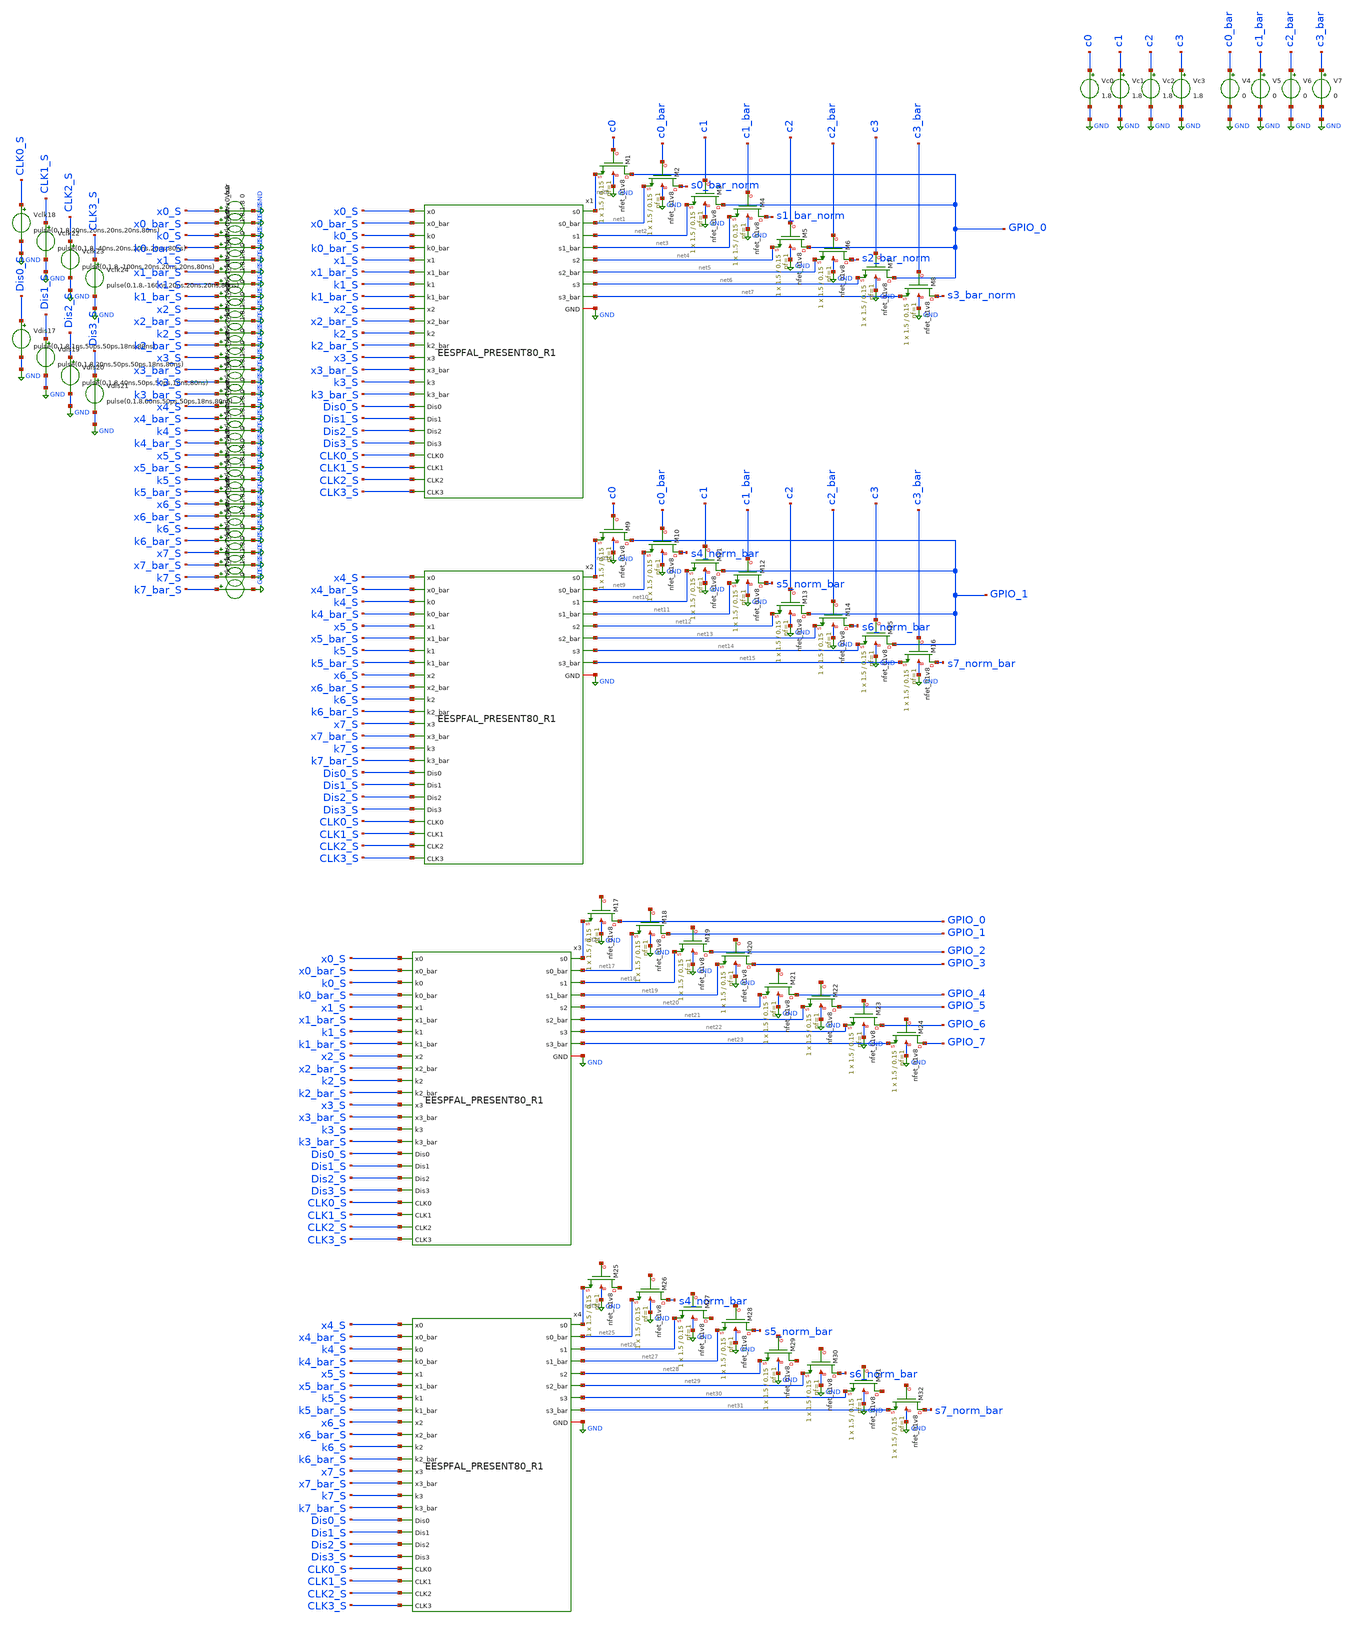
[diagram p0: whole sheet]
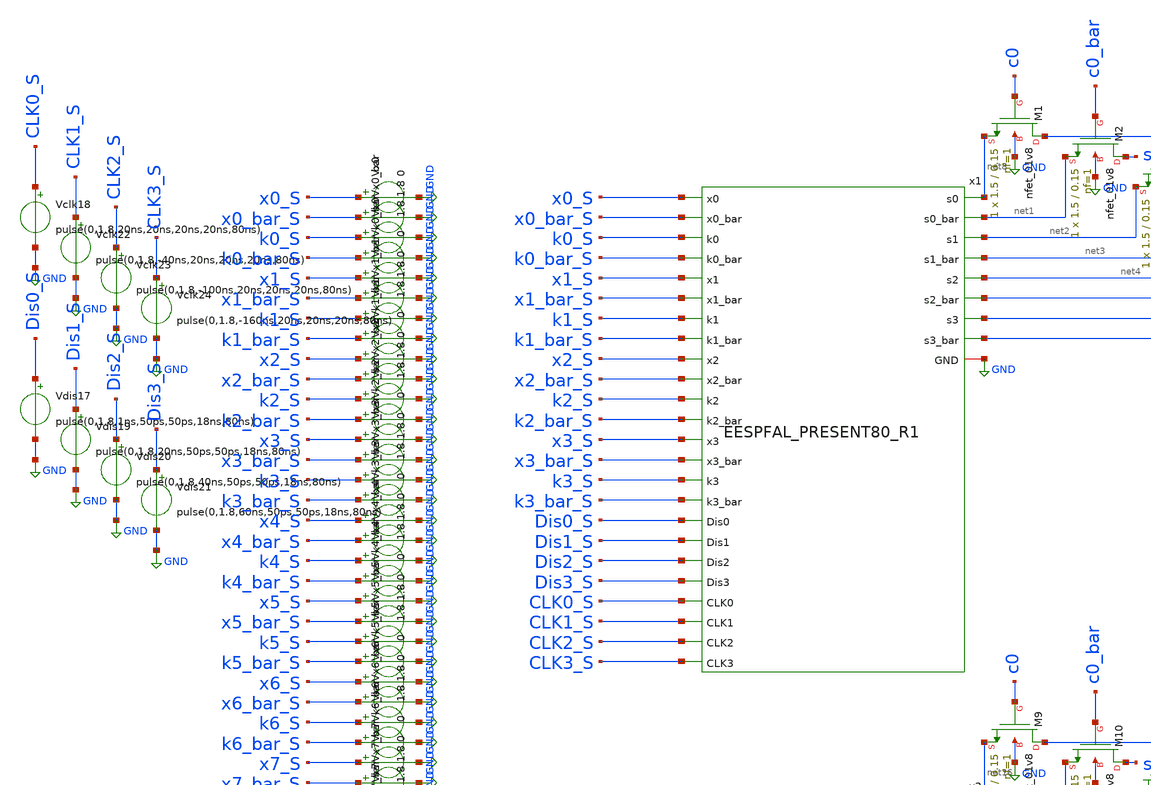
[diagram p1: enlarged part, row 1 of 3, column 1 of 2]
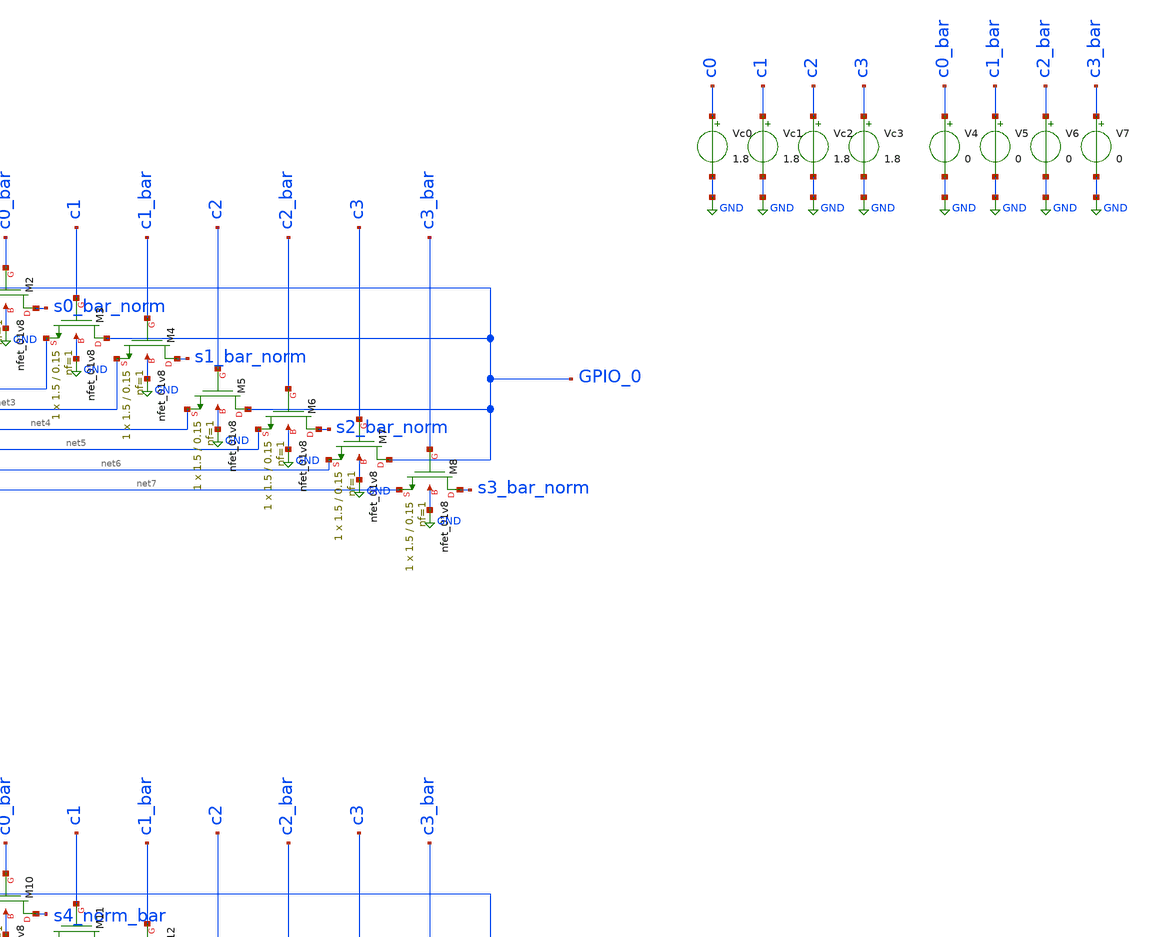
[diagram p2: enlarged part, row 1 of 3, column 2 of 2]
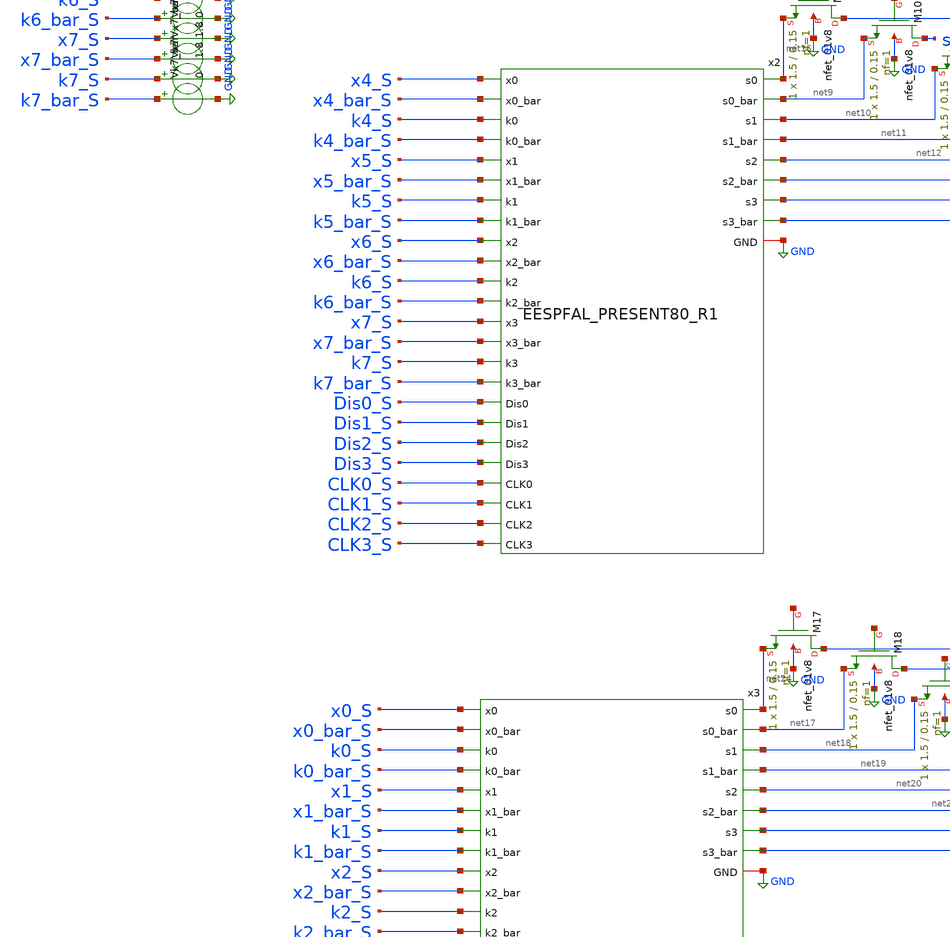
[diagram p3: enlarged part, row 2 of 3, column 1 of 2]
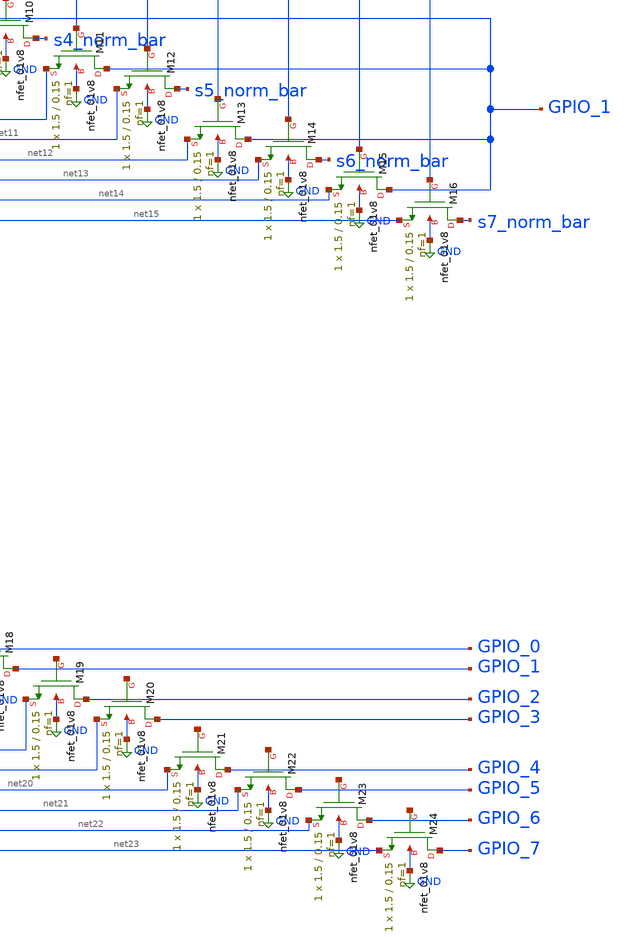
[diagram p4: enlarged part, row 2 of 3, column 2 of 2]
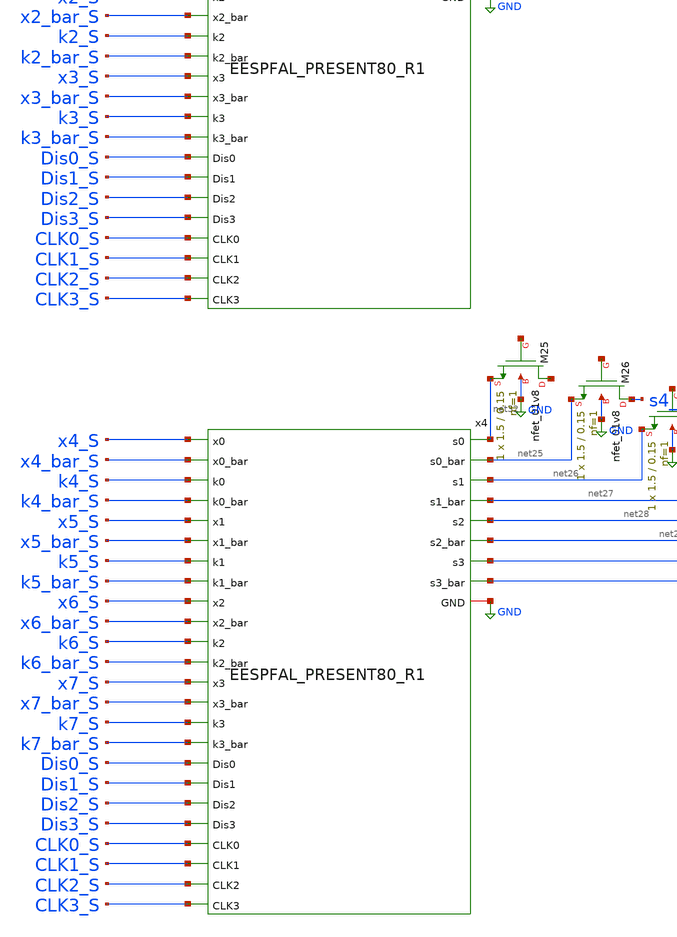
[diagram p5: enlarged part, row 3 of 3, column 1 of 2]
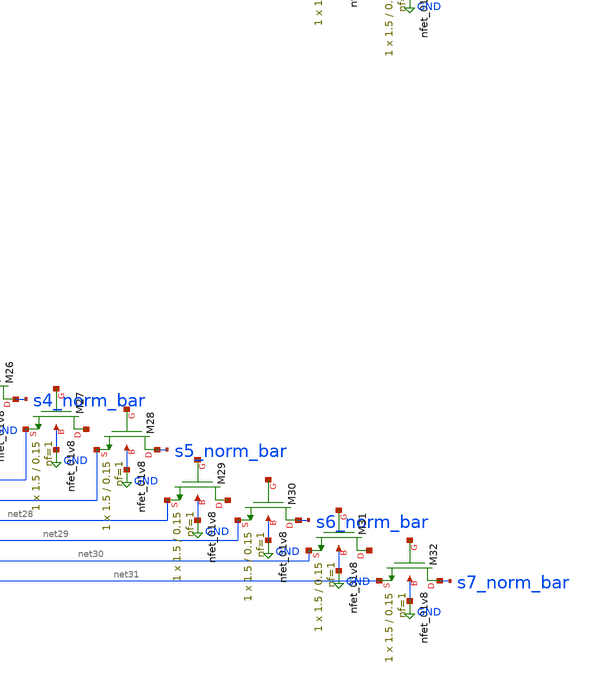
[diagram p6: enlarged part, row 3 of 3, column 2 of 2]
** sch_path: skywater_stuff/EESPFAL_PRESENT80_R1_select_output.sch
**.subckt EESPFAL_PRESENT80_R1_select_output
Vdis17 Dis0_S GND pulse(0,1.8,1ns,50ps,50ps,18ns,80ns)
Vclk18 CLK0_S GND pulse(0,1.8,20ns,20ns,20ns,20ns,80ns)
Vdis19 Dis1_S GND pulse(0,1.8,20ns,50ps,50ps,18ns,80ns)
Vdis20 Dis2_S GND pulse(0,1.8,40ns,50ps,50ps,18ns,80ns)
Vdis21 Dis3_S GND pulse(0,1.8,60ns,50ps,50ps,18ns,80ns)
Vclk22 CLK1_S GND pulse(0,1.8,-40ns,20ns,20ns,20ns,80ns)
Vclk23 CLK2_S GND pulse(0,1.8,-100ns,20ns,20ns,20ns,80ns)
Vclk24 CLK3_S GND pulse(0,1.8,-160ns,20ns,20ns,20ns,80ns)
Vx0 x0_S GND 0
Vx0_bar x0_bar_S GND 1.8
Vk0 k0_S GND 1.8
Vk0_bar k0_bar_S GND 0
Vx1 x1_S GND 0
Vx1_bar x1_bar_S GND 1.8
Vk1 k1_S GND 1.8
Vk1_bar k1_bar_S GND 0
Vx2 x2_S GND 0
Vx2_bar x2_bar_S GND 1.8
Vk2 k2_S GND 1.8
Vk2_bar k2_bar_S GND 0
Vx3 x3_S GND 0
Vx3_bar x3_bar_S GND 1.8
Vk3 k3_S GND 1.8
Vk3_bar k3_bar_S GND 0
Vx4 x4_S GND 0
Vx4_bar x4_bar_S GND 1.8
Vk4 k4_S GND 1.8
Vk4_bar k4_bar_S GND 0
Vx5 x5_S GND 0
Vx5_bar x5_bar_S GND 1.8
Vk5 k5_S GND 1.8
Vk5_bar k5_bar_S GND 0
Vx6 x6_S GND 0
Vx6_bar x6_bar_S GND 1.8
Vk6 k6_S GND 1.8
Vk6_bar k6_bar_S GND 0
Vx7 x7_S GND 0
Vx7_bar x7_bar_S GND 1.8
Vk7 k7_S GND 1.8
Vk7_bar k7_bar_S GND 0
x1 GND x0_S x0_bar_S k0_S k0_bar_S x1_S x1_bar_S k1_S k1_bar_S x2_S x2_bar_S k2_S k2_bar_S x3_S
+ x3_bar_S k3_S k3_bar_S net8 net1 CLK0_S Dis0_S CLK1_S Dis1_S net4 net5 net7 net6 net3 net2 CLK3_S Dis2_S
+ CLK2_S Dis3_S EESPFAL_PRESENT80_R1
x2 GND x4_S x4_bar_S k4_S k4_bar_S x5_S x5_bar_S k5_S k5_bar_S x6_S x6_bar_S k6_S k6_bar_S x7_S
+ x7_bar_S k7_S k7_bar_S net16 net9 CLK0_S Dis0_S CLK1_S Dis1_S net12 net13 net15 net14 net11 net10 CLK3_S
+ Dis2_S CLK2_S Dis3_S EESPFAL_PRESENT80_R1
XM1 GPIO_0 c0 net8 GND sky130_fd_pr__nfet_01v8 L=0.15 W=1.5 nf=1 ad='int((nf+1)/2) * W/nf * 0.29' as='int((nf+2)/2) * W/nf * 0.29'
+ pd='2*int((nf+1)/2) * (W/nf + 0.29)' ps='2*int((nf+2)/2) * (W/nf + 0.29)' nrd='0.29 / W' nrs='0.29 / W'
+ sa=0 sb=0 sd=0 mult=1 m=1
XM2 s0_bar_norm c0_bar net1 GND sky130_fd_pr__nfet_01v8 L=0.15 W=1.5 nf=1 ad='int((nf+1)/2) * W/nf * 0.29'
+ as='int((nf+2)/2) * W/nf * 0.29' pd='2*int((nf+1)/2) * (W/nf + 0.29)' ps='2*int((nf+2)/2) * (W/nf + 0.29)'
+ nrd='0.29 / W' nrs='0.29 / W' sa=0 sb=0 sd=0 mult=1 m=1
XM3 GPIO_0 c1 net2 GND sky130_fd_pr__nfet_01v8 L=0.15 W=1.5 nf=1 ad='int((nf+1)/2) * W/nf * 0.29' as='int((nf+2)/2) * W/nf * 0.29'
+ pd='2*int((nf+1)/2) * (W/nf + 0.29)' ps='2*int((nf+2)/2) * (W/nf + 0.29)' nrd='0.29 / W' nrs='0.29 / W'
+ sa=0 sb=0 sd=0 mult=1 m=1
XM4 s1_bar_norm c1_bar net3 GND sky130_fd_pr__nfet_01v8 L=0.15 W=1.5 nf=1 ad='int((nf+1)/2) * W/nf * 0.29'
+ as='int((nf+2)/2) * W/nf * 0.29' pd='2*int((nf+1)/2) * (W/nf + 0.29)' ps='2*int((nf+2)/2) * (W/nf + 0.29)'
+ nrd='0.29 / W' nrs='0.29 / W' sa=0 sb=0 sd=0 mult=1 m=1
XM5 GPIO_0 c2 net4 GND sky130_fd_pr__nfet_01v8 L=0.15 W=1.5 nf=1 ad='int((nf+1)/2) * W/nf * 0.29' as='int((nf+2)/2) * W/nf * 0.29'
+ pd='2*int((nf+1)/2) * (W/nf + 0.29)' ps='2*int((nf+2)/2) * (W/nf + 0.29)' nrd='0.29 / W' nrs='0.29 / W'
+ sa=0 sb=0 sd=0 mult=1 m=1
XM6 s2_bar_norm c2_bar net5 GND sky130_fd_pr__nfet_01v8 L=0.15 W=1.5 nf=1 ad='int((nf+1)/2) * W/nf * 0.29'
+ as='int((nf+2)/2) * W/nf * 0.29' pd='2*int((nf+1)/2) * (W/nf + 0.29)' ps='2*int((nf+2)/2) * (W/nf + 0.29)'
+ nrd='0.29 / W' nrs='0.29 / W' sa=0 sb=0 sd=0 mult=1 m=1
XM7 GPIO_0 c3 net6 GND sky130_fd_pr__nfet_01v8 L=0.15 W=1.5 nf=1 ad='int((nf+1)/2) * W/nf * 0.29' as='int((nf+2)/2) * W/nf * 0.29'
+ pd='2*int((nf+1)/2) * (W/nf + 0.29)' ps='2*int((nf+2)/2) * (W/nf + 0.29)' nrd='0.29 / W' nrs='0.29 / W'
+ sa=0 sb=0 sd=0 mult=1 m=1
XM8 s3_bar_norm c3_bar net7 GND sky130_fd_pr__nfet_01v8 L=0.15 W=1.5 nf=1 ad='int((nf+1)/2) * W/nf * 0.29'
+ as='int((nf+2)/2) * W/nf * 0.29' pd='2*int((nf+1)/2) * (W/nf + 0.29)' ps='2*int((nf+2)/2) * (W/nf + 0.29)'
+ nrd='0.29 / W' nrs='0.29 / W' sa=0 sb=0 sd=0 mult=1 m=1
XM9 GPIO_1 c0 net16 GND sky130_fd_pr__nfet_01v8 L=0.15 W=1.5 nf=1 ad='int((nf+1)/2) * W/nf * 0.29' as='int((nf+2)/2) * W/nf * 0.29'
+ pd='2*int((nf+1)/2) * (W/nf + 0.29)' ps='2*int((nf+2)/2) * (W/nf + 0.29)' nrd='0.29 / W' nrs='0.29 / W'
+ sa=0 sb=0 sd=0 mult=1 m=1
XM10 s4_norm_bar c0_bar net9 GND sky130_fd_pr__nfet_01v8 L=0.15 W=1.5 nf=1 ad='int((nf+1)/2) * W/nf * 0.29'
+ as='int((nf+2)/2) * W/nf * 0.29' pd='2*int((nf+1)/2) * (W/nf + 0.29)' ps='2*int((nf+2)/2) * (W/nf + 0.29)'
+ nrd='0.29 / W' nrs='0.29 / W' sa=0 sb=0 sd=0 mult=1 m=1
XM11 GPIO_1 c1 net10 GND sky130_fd_pr__nfet_01v8 L=0.15 W=1.5 nf=1 ad='int((nf+1)/2) * W/nf * 0.29' as='int((nf+2)/2) * W/nf * 0.29'
+ pd='2*int((nf+1)/2) * (W/nf + 0.29)' ps='2*int((nf+2)/2) * (W/nf + 0.29)' nrd='0.29 / W' nrs='0.29 / W'
+ sa=0 sb=0 sd=0 mult=1 m=1
XM12 s5_norm_bar c1_bar net11 GND sky130_fd_pr__nfet_01v8 L=0.15 W=1.5 nf=1 ad='int((nf+1)/2) * W/nf * 0.29'
+ as='int((nf+2)/2) * W/nf * 0.29' pd='2*int((nf+1)/2) * (W/nf + 0.29)' ps='2*int((nf+2)/2) * (W/nf + 0.29)'
+ nrd='0.29 / W' nrs='0.29 / W' sa=0 sb=0 sd=0 mult=1 m=1
XM13 GPIO_1 c2 net12 GND sky130_fd_pr__nfet_01v8 L=0.15 W=1.5 nf=1 ad='int((nf+1)/2) * W/nf * 0.29' as='int((nf+2)/2) * W/nf * 0.29'
+ pd='2*int((nf+1)/2) * (W/nf + 0.29)' ps='2*int((nf+2)/2) * (W/nf + 0.29)' nrd='0.29 / W' nrs='0.29 / W'
+ sa=0 sb=0 sd=0 mult=1 m=1
XM14 s6_norm_bar c2_bar net13 GND sky130_fd_pr__nfet_01v8 L=0.15 W=1.5 nf=1 ad='int((nf+1)/2) * W/nf * 0.29'
+ as='int((nf+2)/2) * W/nf * 0.29' pd='2*int((nf+1)/2) * (W/nf + 0.29)' ps='2*int((nf+2)/2) * (W/nf + 0.29)'
+ nrd='0.29 / W' nrs='0.29 / W' sa=0 sb=0 sd=0 mult=1 m=1
XM15 GPIO_1 c3 net14 GND sky130_fd_pr__nfet_01v8 L=0.15 W=1.5 nf=1 ad='int((nf+1)/2) * W/nf * 0.29' as='int((nf+2)/2) * W/nf * 0.29'
+ pd='2*int((nf+1)/2) * (W/nf + 0.29)' ps='2*int((nf+2)/2) * (W/nf + 0.29)' nrd='0.29 / W' nrs='0.29 / W'
+ sa=0 sb=0 sd=0 mult=1 m=1
XM16 s7_norm_bar c3_bar net15 GND sky130_fd_pr__nfet_01v8 L=0.15 W=1.5 nf=1 ad='int((nf+1)/2) * W/nf * 0.29'
+ as='int((nf+2)/2) * W/nf * 0.29' pd='2*int((nf+1)/2) * (W/nf + 0.29)' ps='2*int((nf+2)/2) * (W/nf + 0.29)'
+ nrd='0.29 / W' nrs='0.29 / W' sa=0 sb=0 sd=0 mult=1 m=1
Vc0 c0 GND 1.8
Vc1 c1 GND 1.8
Vc2 c2 GND 1.8
Vc3 c3 GND 1.8
V4 c0_bar GND 0
V5 c1_bar GND 0
V6 c2_bar GND 0
V7 c3_bar GND 0
x3 GND x0_S x0_bar_S k0_S k0_bar_S x1_S x1_bar_S k1_S k1_bar_S x2_S x2_bar_S k2_S k2_bar_S x3_S
+ x3_bar_S k3_S k3_bar_S net24 net17 CLK0_S Dis0_S CLK1_S Dis1_S net20 net21 net23 net22 net19 net18 CLK3_S
+ Dis2_S CLK2_S Dis3_S EESPFAL_PRESENT80_R1
x4 GND x4_S x4_bar_S k4_S k4_bar_S x5_S x5_bar_S k5_S k5_bar_S x6_S x6_bar_S k6_S k6_bar_S x7_S
+ x7_bar_S k7_S k7_bar_S net32 net25 CLK0_S Dis0_S CLK1_S Dis1_S net28 net29 net31 net30 net27 net26 CLK3_S
+ Dis2_S CLK2_S Dis3_S EESPFAL_PRESENT80_R1
XM17 GPIO_0 net33 net24 GND sky130_fd_pr__nfet_01v8 L=0.15 W=1.5 nf=1 ad='int((nf+1)/2) * W/nf * 0.29'
+ as='int((nf+2)/2) * W/nf * 0.29' pd='2*int((nf+1)/2) * (W/nf + 0.29)' ps='2*int((nf+2)/2) * (W/nf + 0.29)'
+ nrd='0.29 / W' nrs='0.29 / W' sa=0 sb=0 sd=0 mult=1 m=1
XM18 GPIO_1 net34 net17 GND sky130_fd_pr__nfet_01v8 L=0.15 W=1.5 nf=1 ad='int((nf+1)/2) * W/nf * 0.29'
+ as='int((nf+2)/2) * W/nf * 0.29' pd='2*int((nf+1)/2) * (W/nf + 0.29)' ps='2*int((nf+2)/2) * (W/nf + 0.29)'
+ nrd='0.29 / W' nrs='0.29 / W' sa=0 sb=0 sd=0 mult=1 m=1
XM19 GPIO_2 net35 net18 GND sky130_fd_pr__nfet_01v8 L=0.15 W=1.5 nf=1 ad='int((nf+1)/2) * W/nf * 0.29'
+ as='int((nf+2)/2) * W/nf * 0.29' pd='2*int((nf+1)/2) * (W/nf + 0.29)' ps='2*int((nf+2)/2) * (W/nf + 0.29)'
+ nrd='0.29 / W' nrs='0.29 / W' sa=0 sb=0 sd=0 mult=1 m=1
XM20 GPIO_3 net36 net19 GND sky130_fd_pr__nfet_01v8 L=0.15 W=1.5 nf=1 ad='int((nf+1)/2) * W/nf * 0.29'
+ as='int((nf+2)/2) * W/nf * 0.29' pd='2*int((nf+1)/2) * (W/nf + 0.29)' ps='2*int((nf+2)/2) * (W/nf + 0.29)'
+ nrd='0.29 / W' nrs='0.29 / W' sa=0 sb=0 sd=0 mult=1 m=1
XM21 GPIO_4 net37 net20 GND sky130_fd_pr__nfet_01v8 L=0.15 W=1.5 nf=1 ad='int((nf+1)/2) * W/nf * 0.29'
+ as='int((nf+2)/2) * W/nf * 0.29' pd='2*int((nf+1)/2) * (W/nf + 0.29)' ps='2*int((nf+2)/2) * (W/nf + 0.29)'
+ nrd='0.29 / W' nrs='0.29 / W' sa=0 sb=0 sd=0 mult=1 m=1
XM22 GPIO_5 net38 net21 GND sky130_fd_pr__nfet_01v8 L=0.15 W=1.5 nf=1 ad='int((nf+1)/2) * W/nf * 0.29'
+ as='int((nf+2)/2) * W/nf * 0.29' pd='2*int((nf+1)/2) * (W/nf + 0.29)' ps='2*int((nf+2)/2) * (W/nf + 0.29)'
+ nrd='0.29 / W' nrs='0.29 / W' sa=0 sb=0 sd=0 mult=1 m=1
XM23 GPIO_6 net39 net22 GND sky130_fd_pr__nfet_01v8 L=0.15 W=1.5 nf=1 ad='int((nf+1)/2) * W/nf * 0.29'
+ as='int((nf+2)/2) * W/nf * 0.29' pd='2*int((nf+1)/2) * (W/nf + 0.29)' ps='2*int((nf+2)/2) * (W/nf + 0.29)'
+ nrd='0.29 / W' nrs='0.29 / W' sa=0 sb=0 sd=0 mult=1 m=1
XM24 GPIO_7 net40 net23 GND sky130_fd_pr__nfet_01v8 L=0.15 W=1.5 nf=1 ad='int((nf+1)/2) * W/nf * 0.29'
+ as='int((nf+2)/2) * W/nf * 0.29' pd='2*int((nf+1)/2) * (W/nf + 0.29)' ps='2*int((nf+2)/2) * (W/nf + 0.29)'
+ nrd='0.29 / W' nrs='0.29 / W' sa=0 sb=0 sd=0 mult=1 m=1
XM25 net41 net42 net32 GND sky130_fd_pr__nfet_01v8 L=0.15 W=1.5 nf=1 ad='int((nf+1)/2) * W/nf * 0.29'
+ as='int((nf+2)/2) * W/nf * 0.29' pd='2*int((nf+1)/2) * (W/nf + 0.29)' ps='2*int((nf+2)/2) * (W/nf + 0.29)'
+ nrd='0.29 / W' nrs='0.29 / W' sa=0 sb=0 sd=0 mult=1 m=1
XM26 s4_norm_bar net43 net25 GND sky130_fd_pr__nfet_01v8 L=0.15 W=1.5 nf=1 ad='int((nf+1)/2) * W/nf * 0.29'
+ as='int((nf+2)/2) * W/nf * 0.29' pd='2*int((nf+1)/2) * (W/nf + 0.29)' ps='2*int((nf+2)/2) * (W/nf + 0.29)'
+ nrd='0.29 / W' nrs='0.29 / W' sa=0 sb=0 sd=0 mult=1 m=1
XM27 net44 net45 net26 GND sky130_fd_pr__nfet_01v8 L=0.15 W=1.5 nf=1 ad='int((nf+1)/2) * W/nf * 0.29'
+ as='int((nf+2)/2) * W/nf * 0.29' pd='2*int((nf+1)/2) * (W/nf + 0.29)' ps='2*int((nf+2)/2) * (W/nf + 0.29)'
+ nrd='0.29 / W' nrs='0.29 / W' sa=0 sb=0 sd=0 mult=1 m=1
XM28 s5_norm_bar net46 net27 GND sky130_fd_pr__nfet_01v8 L=0.15 W=1.5 nf=1 ad='int((nf+1)/2) * W/nf * 0.29'
+ as='int((nf+2)/2) * W/nf * 0.29' pd='2*int((nf+1)/2) * (W/nf + 0.29)' ps='2*int((nf+2)/2) * (W/nf + 0.29)'
+ nrd='0.29 / W' nrs='0.29 / W' sa=0 sb=0 sd=0 mult=1 m=1
XM29 net47 net48 net28 GND sky130_fd_pr__nfet_01v8 L=0.15 W=1.5 nf=1 ad='int((nf+1)/2) * W/nf * 0.29'
+ as='int((nf+2)/2) * W/nf * 0.29' pd='2*int((nf+1)/2) * (W/nf + 0.29)' ps='2*int((nf+2)/2) * (W/nf + 0.29)'
+ nrd='0.29 / W' nrs='0.29 / W' sa=0 sb=0 sd=0 mult=1 m=1
XM30 s6_norm_bar net49 net29 GND sky130_fd_pr__nfet_01v8 L=0.15 W=1.5 nf=1 ad='int((nf+1)/2) * W/nf * 0.29'
+ as='int((nf+2)/2) * W/nf * 0.29' pd='2*int((nf+1)/2) * (W/nf + 0.29)' ps='2*int((nf+2)/2) * (W/nf + 0.29)'
+ nrd='0.29 / W' nrs='0.29 / W' sa=0 sb=0 sd=0 mult=1 m=1
XM31 net50 net51 net30 GND sky130_fd_pr__nfet_01v8 L=0.15 W=1.5 nf=1 ad='int((nf+1)/2) * W/nf * 0.29'
+ as='int((nf+2)/2) * W/nf * 0.29' pd='2*int((nf+1)/2) * (W/nf + 0.29)' ps='2*int((nf+2)/2) * (W/nf + 0.29)'
+ nrd='0.29 / W' nrs='0.29 / W' sa=0 sb=0 sd=0 mult=1 m=1
XM32 s7_norm_bar net52 net31 GND sky130_fd_pr__nfet_01v8 L=0.15 W=1.5 nf=1 ad='int((nf+1)/2) * W/nf * 0.29'
+ as='int((nf+2)/2) * W/nf * 0.29' pd='2*int((nf+1)/2) * (W/nf + 0.29)' ps='2*int((nf+2)/2) * (W/nf + 0.29)'
+ nrd='0.29 / W' nrs='0.29 / W' sa=0 sb=0 sd=0 mult=1 m=1
**** begin user architecture code

.lib /research/pdk/open_pdks/share/pdk/sky130A/libs.tech/ngspice/sky130.lib.spice tt
**.include ~/magic_layout_stuff/EESPFAL_PRESENT80_R1.spice
**.include ~/magic_layout_stuff/EESPFAL_PRESENT80_R1_flat.spice
.param v0 ='0' v0_bar ='1.8' v1 ='0' v1_bar ='1.8' v2 ='0' v2_bar ='1.8' v3 ='0' v3_bar ='1.8'
.option method=gear
.control
echo We at start now
set tstart=0
*set tstop=0
let index=0
let index2=1
let wstart = $tstart
let wstop = 0n
let key = 7
let total_time = 32
let cycle_index = 1

*foreach bit_index 0 1 2 3
*	set bit = `./test.sh $&key $bit_index`
*	alter Vc$bit_index = '$bit ? 1.8 : 0'
*	alter Vk`echo $bit_index`_bar = '$bit ? 0 : 1.8'
*end

let bit_index = 0
while bit_index < 8
	set bit = `./test.sh $&key $&bit_index`
	alter Vk$&bit_index = '$bit ? 1.8 : 0'
	alter Vk`echo $&bit_index`_bar = '$bit ? 0 : 1.8'
	let bit_index = bit_index + 1
end

*set values_raw < circ_inputs_`echo $&cycle_index`.txt
set values_raw < circ_inputs_not_rand_`echo $&cycle_index`.txt
compose values values $values_raw
echo stuff

*let curr_time = index*80n

while index2 < length(values)
	let wstop = $&index2*80n
	stop when time=$&wstop
	let index2 = $&index2+1
	echo $&index2
end

let tstop = length(values)*80n
while index < length(values)
	let value = values[$&index]
	echo $&value
	echo going into altering
	let bit_index = 0
	while bit_index < 8
		set bit = `./test.sh $&value $&bit_index`
		alter Vx$&bit_index = '$bit ? 1.8 : 0'
		alter Vx`echo $&bit_index`_bar = '$bit ? 0 : 1.8'
		let bit_index = bit_index + 1
	end
	echo test stuff
	let index=index+1
	if index = 1
		tran 1n $&tstop 0 1n
	else
		resume
	end
end

*let Pinst_CLK0_CLK3 =
*+ (v(CLK0_S)*i(vclk18))+(v(CLK1_S)*i(vclk22))+(v(CLK2_S)*i(vclk23))+(v(CLK3_S)*i(vclk24))
*plot Pinst_CLK0_CLK3
let index = 0
while index < length(values)
	let Pinst_CLK0_CLK3 =
+ (v(CLK0_S)*i(vclk18))+(v(CLK1_S)*i(vclk22))+(v(CLK2_S)*i(vclk23))+(v(CLK3_S)*i(vclk24))
	**let Pinst_CLK0_CLK3_Dis0_Dis3 =
+ (v(CLK0_S)*i(vclk18))+(v(CLK1_S)*i(vclk22))+(v(CLK2_S)*i(vclk23))+(v(CLK3_S)*i(vclk24))+(v(Dis0_S)*i(vdis17))+(v(Dis1_S)*i(vdis19))+(v(Dis2_S)*i(vdis20))+(v(Dis3_S)*i(vdis21))
	**plot Pinst_CLK0_CLK3
	let lin-tstart = $&index*80ns
	let lin-tstop = $&lin-tstart+80ns
	let lin-tstep = 0.1n
	linearize Pinst_CLK0_CLK3
	*display
	set appendwrite
	*wrdata EESPFAL_K`echo $&key`_`echo $&total_time`u_`echo $&cycle_index`cycle_norm.csv
+ Pinst_CLK0_CLK3
	*wrdata EESPFAL_FULL_R1_K`echo $&key`_`echo $&total_time`u_`echo $&cycle_index`cycle_norm.csv
+ Pinst_CLK0_CLK3
	*wrdata EESPFAL_32bits_K`echo $&key`_`echo $&total_time`u_`echo $&cycle_index`cycle_norm.csv
+ Pinst_CLK0_CLK3
	*wrdata EESPFAL_K`echo $&key`_`echo $&total_time`u_`echo $&cycle_index`cycle_flat.csv
+ Pinst_CLK0_CLK3
	let index = index + 1
	*echo $plots
	setplot tran1
	destroy tran2
	*echo $plots
end
	plot v(CLK0_S)
	plot v(CLK3_S)
	plot v(s0_norm)
	plot v(s2_norm)
	plot v(s4_norm)
	plot v(s6_norm)
.endc


**** end user architecture code
**.ends
.GLOBAL GND
.end
